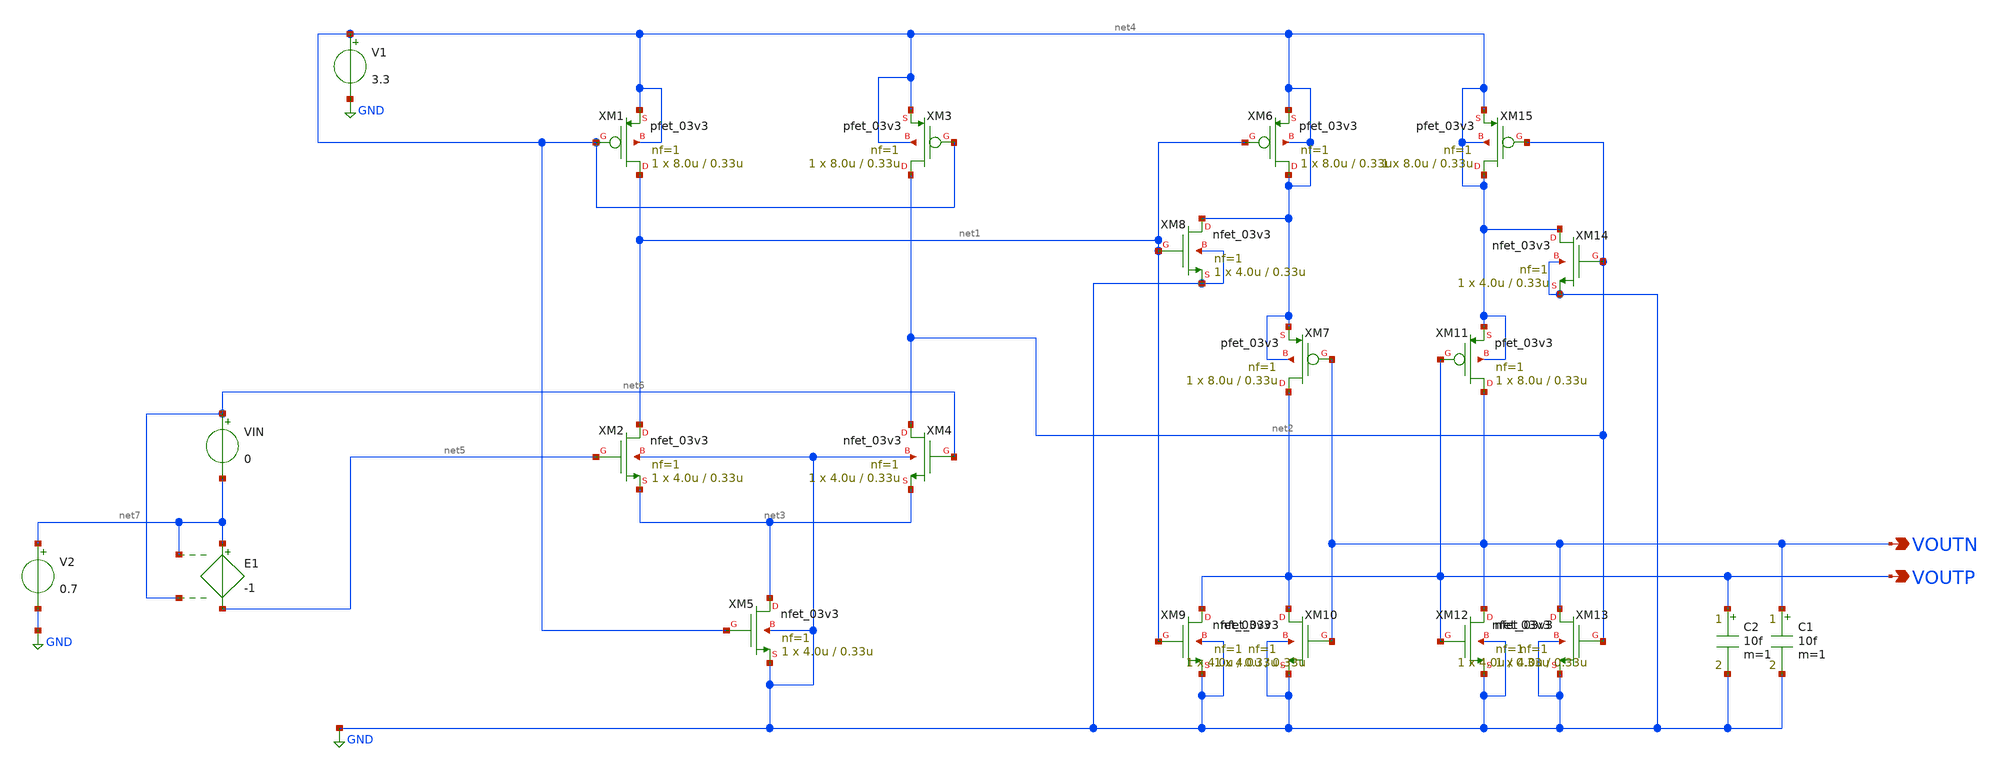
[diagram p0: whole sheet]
** sch_path: noritsuna/comparator/comparator_tb.sch
**.subckt comparator_tb VOUTN VOUTP
*.opin VOUTN
*.opin VOUTP
XM1 net1 net4 net4 net4 pfet_03v3 L=0.33u W=8.0u nf=1 ad='int((nf+1)/2) * W/nf * 0.18u' as='int((nf+2)/2) * W/nf * 0.18u'
+ pd='2*int((nf+1)/2) * (W/nf + 0.18u)' ps='2*int((nf+2)/2) * (W/nf + 0.18u)' nrd='0.18u / W' nrs='0.18u / W'
+ sa=0 sb=0 sd=0 m=1
XM2 net1 net5 net3 GND nfet_03v3 L=0.33u W=4.0u nf=1 ad='int((nf+1)/2) * W/nf * 0.18u' as='int((nf+2)/2) * W/nf * 0.18u'
+ pd='2*int((nf+1)/2) * (W/nf + 0.18u)' ps='2*int((nf+2)/2) * (W/nf + 0.18u)' nrd='0.18u / W' nrs='0.18u / W'
+ sa=0 sb=0 sd=0 m=1
XM3 net2 net4 net4 net4 pfet_03v3 L=0.33u W=8.0u nf=1 ad='int((nf+1)/2) * W/nf * 0.18u' as='int((nf+2)/2) * W/nf * 0.18u'
+ pd='2*int((nf+1)/2) * (W/nf + 0.18u)' ps='2*int((nf+2)/2) * (W/nf + 0.18u)' nrd='0.18u / W' nrs='0.18u / W'
+ sa=0 sb=0 sd=0 m=1
XM4 net2 net6 net3 GND nfet_03v3 L=0.33u W=4.0u nf=1 ad='int((nf+1)/2) * W/nf * 0.18u' as='int((nf+2)/2) * W/nf * 0.18u'
+ pd='2*int((nf+1)/2) * (W/nf + 0.18u)' ps='2*int((nf+2)/2) * (W/nf + 0.18u)' nrd='0.18u / W' nrs='0.18u / W'
+ sa=0 sb=0 sd=0 m=1
XM5 net3 net4 GND GND nfet_03v3 L=0.33u W=4.0u nf=1 ad='int((nf+1)/2) * W/nf * 0.18u' as='int((nf+2)/2) * W/nf * 0.18u'
+ pd='2*int((nf+1)/2) * (W/nf + 0.18u)' ps='2*int((nf+2)/2) * (W/nf + 0.18u)' nrd='0.18u / W' nrs='0.18u / W'
+ sa=0 sb=0 sd=0 m=1
XM6 net4 net1 net4 net4 pfet_03v3 L=0.33u W=8.0u nf=1 ad='int((nf+1)/2) * W/nf * 0.18u' as='int((nf+2)/2) * W/nf * 0.18u'
+ pd='2*int((nf+1)/2) * (W/nf + 0.18u)' ps='2*int((nf+2)/2) * (W/nf + 0.18u)' nrd='0.18u / W' nrs='0.18u / W'
+ sa=0 sb=0 sd=0 m=1
XM7 VOUTP VOUTN net4 net4 pfet_03v3 L=0.33u W=8.0u nf=1 ad='int((nf+1)/2) * W/nf * 0.18u' as='int((nf+2)/2) * W/nf * 0.18u'
+ pd='2*int((nf+1)/2) * (W/nf + 0.18u)' ps='2*int((nf+2)/2) * (W/nf + 0.18u)' nrd='0.18u / W' nrs='0.18u / W'
+ sa=0 sb=0 sd=0 m=1
XM8 net4 net1 GND GND nfet_03v3 L=0.33u W=4.0u nf=1 ad='int((nf+1)/2) * W/nf * 0.18u' as='int((nf+2)/2) * W/nf * 0.18u'
+ pd='2*int((nf+1)/2) * (W/nf + 0.18u)' ps='2*int((nf+2)/2) * (W/nf + 0.18u)' nrd='0.18u / W' nrs='0.18u / W'
+ sa=0 sb=0 sd=0 m=1
XM9 VOUTP net1 GND GND nfet_03v3 L=0.33u W=4.0u nf=1 ad='int((nf+1)/2) * W/nf * 0.18u' as='int((nf+2)/2) * W/nf * 0.18u'
+ pd='2*int((nf+1)/2) * (W/nf + 0.18u)' ps='2*int((nf+2)/2) * (W/nf + 0.18u)' nrd='0.18u / W' nrs='0.18u / W'
+ sa=0 sb=0 sd=0 m=1
XM10 VOUTP VOUTN GND GND nfet_03v3 L=0.33u W=4.0u nf=1 ad='int((nf+1)/2) * W/nf * 0.18u' as='int((nf+2)/2) * W/nf * 0.18u'
+ pd='2*int((nf+1)/2) * (W/nf + 0.18u)' ps='2*int((nf+2)/2) * (W/nf + 0.18u)' nrd='0.18u / W' nrs='0.18u / W'
+ sa=0 sb=0 sd=0 m=1
XM11 VOUTN VOUTP net4 net4 pfet_03v3 L=0.33u W=8.0u nf=1 ad='int((nf+1)/2) * W/nf * 0.18u' as='int((nf+2)/2) * W/nf * 0.18u'
+ pd='2*int((nf+1)/2) * (W/nf + 0.18u)' ps='2*int((nf+2)/2) * (W/nf + 0.18u)' nrd='0.18u / W' nrs='0.18u / W'
+ sa=0 sb=0 sd=0 m=1
XM12 VOUTN VOUTP GND GND nfet_03v3 L=0.33u W=4.0u nf=1 ad='int((nf+1)/2) * W/nf * 0.18u' as='int((nf+2)/2) * W/nf * 0.18u'
+ pd='2*int((nf+1)/2) * (W/nf + 0.18u)' ps='2*int((nf+2)/2) * (W/nf + 0.18u)' nrd='0.18u / W' nrs='0.18u / W'
+ sa=0 sb=0 sd=0 m=1
XM13 VOUTN net2 GND GND nfet_03v3 L=0.33u W=4.0u nf=1 ad='int((nf+1)/2) * W/nf * 0.18u' as='int((nf+2)/2) * W/nf * 0.18u'
+ pd='2*int((nf+1)/2) * (W/nf + 0.18u)' ps='2*int((nf+2)/2) * (W/nf + 0.18u)' nrd='0.18u / W' nrs='0.18u / W'
+ sa=0 sb=0 sd=0 m=1
XM14 net4 net2 GND GND nfet_03v3 L=0.33u W=4.0u nf=1 ad='int((nf+1)/2) * W/nf * 0.18u' as='int((nf+2)/2) * W/nf * 0.18u'
+ pd='2*int((nf+1)/2) * (W/nf + 0.18u)' ps='2*int((nf+2)/2) * (W/nf + 0.18u)' nrd='0.18u / W' nrs='0.18u / W'
+ sa=0 sb=0 sd=0 m=1
XM15 net4 net2 net4 net4 pfet_03v3 L=0.33u W=8.0u nf=1 ad='int((nf+1)/2) * W/nf * 0.18u' as='int((nf+2)/2) * W/nf * 0.18u'
+ pd='2*int((nf+1)/2) * (W/nf + 0.18u)' ps='2*int((nf+2)/2) * (W/nf + 0.18u)' nrd='0.18u / W' nrs='0.18u / W'
+ sa=0 sb=0 sd=0 m=1
V1 net4 GND 3.3
VIN net6 net7 0
E1 net7 net5 net7 net6 -1
V2 net7 GND 0.7
C1 VOUTN GND 10f m=1
C2 VOUTP GND 10f m=1
**** begin user architecture code

.include $::180MCU_MODELS/design.ngspice
.lib $::180MCU_MODELS/sm141064.ngspice typical




VDD CLK 0 pulse (0 3.3 0 40p 40p 62.5n 125n) dc 0v
.control
save all
let VSTART = 0
let VSTOP  = 10m
let VDELTA = 0.5m
let v_act   = 0
let i = 0;
while v_act < VSTOP
	tran 0.1n 40n
	alter VIN = v_act
	let v_act = v_act + VDELTA
	write comparator_tb.raw
	set appendwrite
end
.endc



**** end user architecture code
**.ends
.GLOBAL GND
.end
